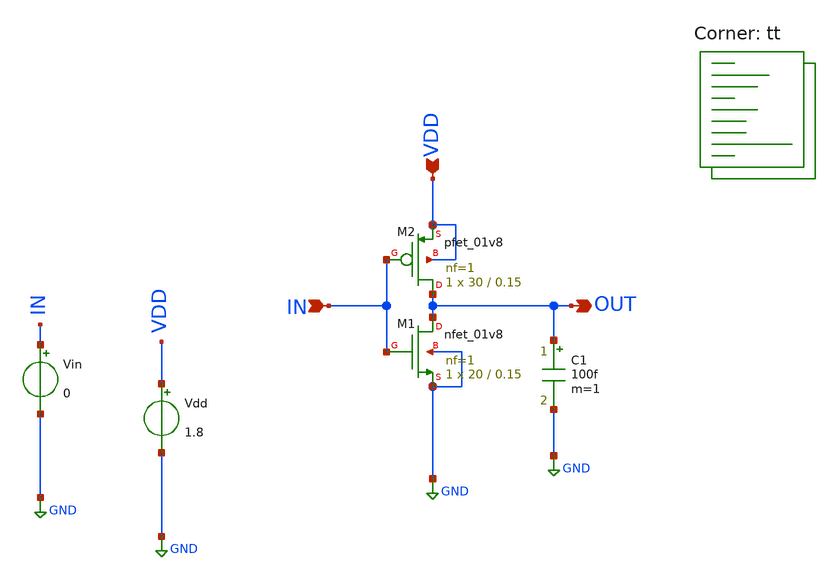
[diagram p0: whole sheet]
** sch_path: sizing-inverter.sch
**.subckt sizing-inverter IN VDD OUT
*.ipin IN
*.ipin VDD
*.opin OUT
Vin IN GND 0
Vdd VDD GND 1.8
XM1 OUT IN GND GND sky130_fd_pr__nfet_01v8 L=0.15 W=20 nf=1 ad='int((nf+1)/2) * W/nf * 0.29' as='int((nf+2)/2) * W/nf * 0.29'
+ pd='2*int((nf+1)/2) * (W/nf + 0.29)' ps='2*int((nf+2)/2) * (W/nf + 0.29)' nrd='0.29 / W' nrs='0.29 / W'
+ sa=0 sb=0 sd=0 mult=1 m=1
XM2 OUT IN VDD VDD sky130_fd_pr__pfet_01v8 L=0.15 W=30 nf=1 ad='int((nf+1)/2) * W/nf * 0.29' as='int((nf+2)/2) * W/nf * 0.29'
+ pd='2*int((nf+1)/2) * (W/nf + 0.29)' ps='2*int((nf+2)/2) * (W/nf + 0.29)' nrd='0.29 / W' nrs='0.29 / W'
+ sa=0 sb=0 sd=0 mult=1 m=1
C1 OUT GND 100f m=1
**** begin user architecture code
.lib $::SKYWATER_MODELS/sky130.lib.spice tt


.options savecurrents
.control
save all


let step=0.1
let max_w=0.8
let curr_w=0.3

let min_diff=100
let best_w=curr_w

while curr_w < max_w
	alter m.xm2.msky130_fd_pr__pfet_01v8 W=curr_w
	reset
	dc vin 0 1.8 1m
	plot v(in) v(out)

	meas dc switching_point WHEN v(out)=v(in) CROSS=LAST

	let difference=abs(switching_point - 0.9)
	print switching_point

	if difference < min_diff
		let best_w = curr_w
		let min_diff = difference
	end

	let curr_w=curr_w + step


end

*print min_diff
*print best_w




.endc


**** end user architecture code
**.ends
.GLOBAL GND
.end
